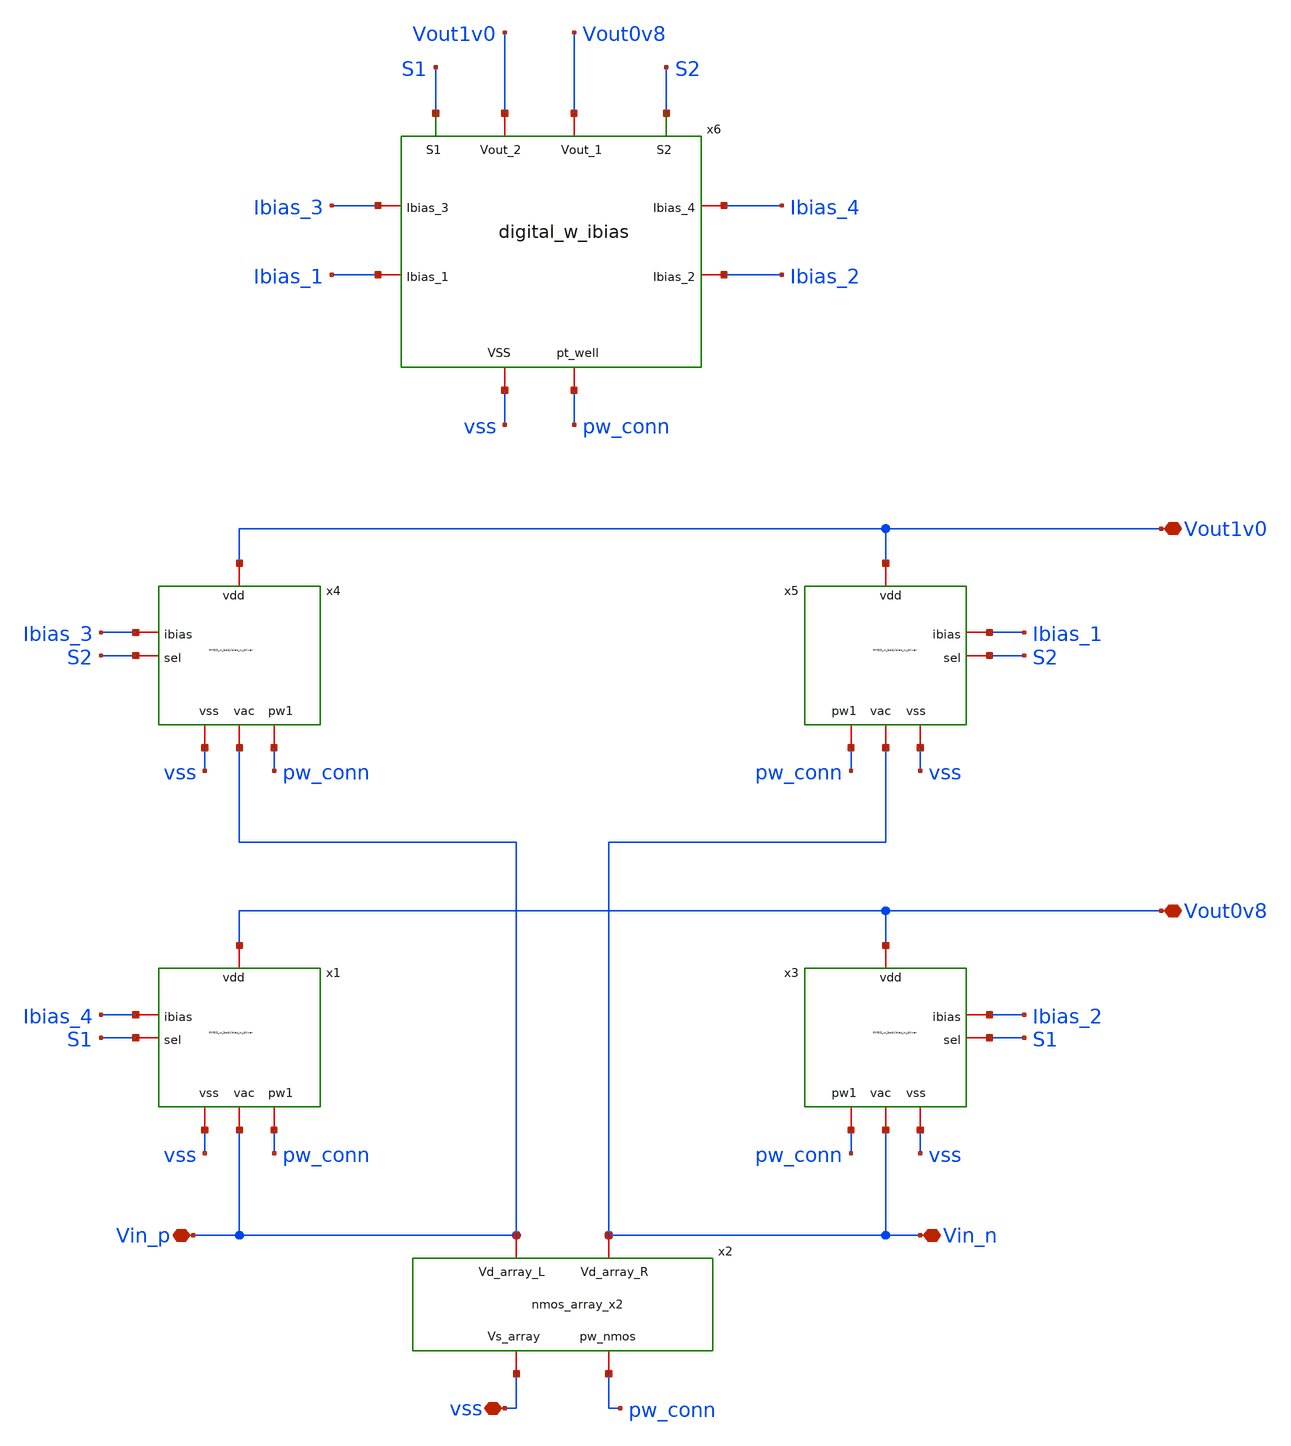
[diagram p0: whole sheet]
** sch_path: Layouts/Top/top_integration_SSDOR.sch
**.subckt top_integration_SSDOR vss Vout0v8 Vout1v0 Vin_n Vin_p
*.iopin vss
*.iopin Vout0v8
*.iopin Vout1v0
*.iopin Vin_n
*.iopin Vin_p
x1 Vout0v8 Vin_p Ibias_4 S1 vss pw_conn PMOS_w_bodybias_w_driver
x2 Vin_p Vin_n pw_conn vss nmos_array_x2
x3 Vout0v8 Vin_n Ibias_2 S1 vss pw_conn PMOS_w_bodybias_w_driver
x4 Vout1v0 Vin_p Ibias_3 S2 vss pw_conn PMOS_w_bodybias_w_driver
x5 Vout1v0 Vin_n Ibias_1 S2 vss pw_conn PMOS_w_bodybias_w_driver
x6 Vout1v0 Vout0v8 S1 vss S2 Ibias_3 Ibias_2 Ibias_4 Ibias_1 pw_conn digital_w_ibias
**.ends

* expanding   symbol:  /shared/designs/Layouts/PMOS/PMOS_w_bodybias_w_driver.sym # of pins=6
** sym_path: Layouts/PMOS/PMOS_w_bodybias_w_driver.sym
** sch_path: Layouts/PMOS/PMOS_w_bodybias_w_driver.sch
.subckt PMOS_w_bodybias_w_driver vdd vac ibias sel vss pw1
*.iopin vdd
*.iopin ibias
*.iopin vac
*.iopin vss
*.iopin sel
*.iopin pw1
XM1 net1 vac vdd net2 sg13_lv_pmos w=9u l=0.13u ng=1 m=1 mm_ok=1
XM2 net1 vdd vac net2 sg13_lv_pmos w=3u l=0.13u ng=1 m=1 mm_ok=1
XR2 net1 net2 ntap1 R=65.77 w=0.7e-6 l=5e-6
XM3 vac net3 vdd net4 sg13_lv_pmos w=86.4u l=0.13u ng=36 m=1 mm_ok=1
XM4 vac net3 vdd net4 sg13_lv_pmos w=86.4u l=0.13u ng=36 m=1 mm_ok=1
XM5 vac net3 vdd net4 sg13_lv_pmos w=86.4u l=0.13u ng=36 m=1 mm_ok=1
XM6 vac net3 vdd net4 sg13_lv_pmos w=86.4u l=0.13u ng=36 m=1 mm_ok=1
XM7 vac net3 vdd net4 sg13_lv_pmos w=86.4u l=0.13u ng=36 m=1 mm_ok=1
XM8 vac net3 vdd net4 sg13_lv_pmos w=86.4u l=0.13u ng=36 m=1 mm_ok=1
XM9 vac net3 vdd net4 sg13_lv_pmos w=86.4u l=0.13u ng=36 m=1 mm_ok=1
XM10 vac net3 vdd net4 sg13_lv_pmos w=86.4u l=0.13u ng=36 m=1 mm_ok=1
XM11 vac net3 vdd net4 sg13_lv_pmos w=86.4u l=0.13u ng=36 m=1 mm_ok=1
XM12 vac net3 vdd net4 sg13_lv_pmos w=86.4u l=0.13u ng=36 m=1 mm_ok=1
XM13 vac net3 vdd net4 sg13_lv_pmos w=86.4u l=0.13u ng=36 m=1 mm_ok=1
XM14 vac net3 vdd net4 sg13_lv_pmos w=86.4u l=0.13u ng=36 m=1 mm_ok=1
XM15 vac net3 vdd net4 sg13_lv_pmos w=86.4u l=0.13u ng=36 m=1 mm_ok=1
XM16 vac net3 vdd net4 sg13_lv_pmos w=86.4u l=0.13u ng=36 m=1 mm_ok=1
XM17 vac net3 vdd net4 sg13_lv_pmos w=86.4u l=0.13u ng=36 m=1 mm_ok=1
XM18 vac net3 vdd net4 sg13_lv_pmos w=86.4u l=0.13u ng=36 m=1 mm_ok=1
XR9 net1 net4 ntap1 R=1.116 w=1e-6 l=292e-6
XR1 net1 net4 ntap1 R=1.116 w=1e-6 l=292e-6
XR3 net1 net4 ntap1 R=1.116 w=1e-6 l=292e-6
XR4 net1 net4 ntap1 R=1.116 w=1e-6 l=292e-6
XR5 net1 net4 ntap1 R=1.116 w=1e-6 l=292e-6
XR6 net1 net4 ntap1 R=1.116 w=1e-6 l=292e-6
XR7 net1 net4 ntap1 R=1.116 w=1e-6 l=292e-6
XR8 net1 net4 ntap1 R=1.116 w=1e-6 l=292e-6
XR10 net1 net4 ntap1 R=1.116 w=1e-6 l=292e-6
XM19 net6 net5 vac nw sg13_lv_pmos w=4u l=0.5u ng=1 m=1 mm_ok=1
XM20 net5 net5 vdd nw sg13_lv_pmos w=4u l=0.5u ng=1 m=1 mm_ok=1
XM21 net7 net8 vdd nw sg13_lv_pmos w=4u l=0.5u ng=1 m=1 mm_ok=1
XM22 net8 net8 vac nw sg13_lv_pmos w=4u l=0.5u ng=1 m=1 mm_ok=1
XM23 net6 net6 vss pw1 sg13_lv_nmos w=1u l=0.5u ng=1 m=1 mm_ok=1
XM24 net7 net6 vss pw1 sg13_lv_nmos w=1u l=0.5u ng=1 m=1 mm_ok=1
XM25 net5 ibias vss pw1 sg13_lv_nmos w=1u l=0.5u ng=1 m=1 mm_ok=1
XM26 ibias ibias vss pw1 sg13_lv_nmos w=1u l=0.5u ng=1 m=1 mm_ok=1
XM27 net8 ibias vss pw1 sg13_lv_nmos w=1u l=0.5u ng=1 m=1 mm_ok=1
XR11 vdd nw ntap1 R=13.24 w=1e-6 l=24e-6
XR12 vdd nw ntap1 R=7.84 w=1.0e-6 l=41e-6
XR13 vdd nw ntap1 R=7.84 w=1.0e-6 l=41e-6
XM28 vdd net10 net9 pw1 sg13_lv_nmos w=1u l=0.13u ng=1 m=1 mm_ok=1
XM29 vdd sel net9 nw sg13_lv_pmos w=2u l=0.13u ng=1 m=1 mm_ok=1
XM30 net7 sel net9 pw1 sg13_lv_nmos w=1u l=0.13u ng=1 m=1 mm_ok=1
XM31 net7 net10 net9 nw sg13_lv_pmos w=2u l=0.13u ng=1 m=1 mm_ok=1
XM32 net11 net9 vss pw1 sg13_lv_nmos w=1u l=0.13u ng=1 m=1 mm_ok=1
XM33 net11 net9 vdd nw sg13_lv_pmos w=1u l=0.13u ng=1 m=2 mm_ok=1
XM34 net12 net11 vss pw1 sg13_lv_nmos w=1u l=0.13u ng=1 m=2 mm_ok=1
XM35 net12 net11 vdd nw sg13_lv_pmos w=1u l=0.13u ng=1 m=4 mm_ok=1
XM36 net13 net12 vss pw1 sg13_lv_nmos w=1u l=0.13u ng=1 m=8 mm_ok=1
XM37 net13 net12 vdd nw sg13_lv_pmos w=1u l=0.13u ng=1 m=16 mm_ok=1
XM38 net3 net13 vdd nw sg13_lv_pmos w=1u l=0.13u ng=1 m=54 mm_ok=1
XM39 net3 net13 vss pw1 sg13_lv_nmos w=1u l=0.13u ng=1 m=27 mm_ok=1
XR14 vdd nw ntap1 R=89.09 w=3e-6 l=1e-6
XR15 vdd nw ntap1 R=196 w=1e-6 l=1e-6
XR16 vdd nw ntap1 R=122.5 w=2e-6 l=1e-6
XR17 vdd nw ntap1 R=122.5 w=2e-6 l=1e-6
XR18 vss pw1 ptap1 R=13.8 w=23.0e-6 l=1.0e-6
XR19 vss pw1 ptap1 R=20.85 w=1.0e-6 l=15.0e-6
XR20 vss pw1 ptap1 R=14.41 w=1.0e-6 l=22.0e-6
XR21 vss pw1 ptap1 R=14.41 w=1.0e-6 l=22.0e-6
XM40 net10 sel vss pw1 sg13_lv_nmos w=0.5u l=0.13u ng=1 m=1 mm_ok=1
XM41 net10 sel vdd nw sg13_lv_pmos w=1u l=0.13u ng=1 m=1 mm_ok=1
.ends


* expanding   symbol:  /shared/designs/Layouts/PMOS/nmos_array_x2.sym # of pins=4
** sym_path: Layouts/PMOS/nmos_array_x2.sym
** sch_path: Layouts/PMOS/nmos_array_x2.sch
.subckt nmos_array_x2 Vd_array_L Vd_array_R pw_nmos Vs_array
*.iopin Vd_array_L
*.iopin Vd_array_R
*.iopin pw_nmos
*.iopin Vs_array
XM2 Vd_array_L Vd_array_R Vs_array pw_nmos sg13_lv_nmos w=86.4u l=0.13u ng=36 m=1 mm_ok=1
XR2 Vs_array pw_nmos ptap1 R=1.529 w=1e-6 l=213e-6
XM1 Vd_array_L Vd_array_R Vs_array pw_nmos sg13_lv_nmos w=86.4u l=0.13u ng=36 m=1 mm_ok=1
XM3 Vd_array_L Vd_array_R Vs_array pw_nmos sg13_lv_nmos w=86.4u l=0.13u ng=36 m=1 mm_ok=1
XM4 Vd_array_L Vd_array_R Vs_array pw_nmos sg13_lv_nmos w=86.4u l=0.13u ng=36 m=1 mm_ok=1
XM5 Vd_array_L Vd_array_R Vs_array pw_nmos sg13_lv_nmos w=86.4u l=0.13u ng=36 m=1 mm_ok=1
XM6 Vd_array_L Vd_array_R Vs_array pw_nmos sg13_lv_nmos w=86.4u l=0.13u ng=36 m=1 mm_ok=1
XM7 Vd_array_L Vd_array_R Vs_array pw_nmos sg13_lv_nmos w=86.4u l=0.13u ng=36 m=1 mm_ok=1
XM8 Vd_array_L Vd_array_R Vs_array pw_nmos sg13_lv_nmos w=86.4u l=0.13u ng=36 m=1 mm_ok=1
XM9 Vd_array_L Vd_array_R Vs_array pw_nmos sg13_lv_nmos w=86.4u l=0.13u ng=36 m=1 mm_ok=1
XR1 Vs_array pw_nmos ptap1 R=1.529 w=1e-6 l=213e-6
XR3 Vs_array pw_nmos ptap1 R=1.529 w=1e-6 l=213e-6
XR4 Vs_array pw_nmos ptap1 R=1.529 w=1e-6 l=213e-6
XR5 Vs_array pw_nmos ptap1 R=1.529 w=1e-6 l=213e-6
XR6 Vs_array pw_nmos ptap1 R=1.529 w=1e-6 l=213e-6
XR7 Vs_array pw_nmos ptap1 R=1.529 w=1e-6 l=213e-6
XM10 Vd_array_R Vd_array_L Vs_array pw_nmos sg13_lv_nmos w=86.4u l=0.13u ng=36 m=1 mm_ok=1
XR8 Vs_array pw_nmos ptap1 R=1.529 w=1e-6 l=213e-6
XM11 Vd_array_R Vd_array_L Vs_array pw_nmos sg13_lv_nmos w=86.4u l=0.13u ng=36 m=1 mm_ok=1
XM12 Vd_array_R Vd_array_L Vs_array pw_nmos sg13_lv_nmos w=86.4u l=0.13u ng=36 m=1 mm_ok=1
XM13 Vd_array_R Vd_array_L Vs_array pw_nmos sg13_lv_nmos w=86.4u l=0.13u ng=36 m=1 mm_ok=1
XM14 Vd_array_R Vd_array_L Vs_array pw_nmos sg13_lv_nmos w=86.4u l=0.13u ng=36 m=1 mm_ok=1
XM15 Vd_array_R Vd_array_L Vs_array pw_nmos sg13_lv_nmos w=86.4u l=0.13u ng=36 m=1 mm_ok=1
XM16 Vd_array_R Vd_array_L Vs_array pw_nmos sg13_lv_nmos w=86.4u l=0.13u ng=36 m=1 mm_ok=1
XM17 Vd_array_R Vd_array_L Vs_array pw_nmos sg13_lv_nmos w=86.4u l=0.13u ng=36 m=1 mm_ok=1
XM18 Vd_array_R Vd_array_L Vs_array pw_nmos sg13_lv_nmos w=86.4u l=0.13u ng=36 m=1 mm_ok=1
XR9 Vs_array pw_nmos ptap1 R=1.529 w=1e-6 l=213e-6
XR10 Vs_array pw_nmos ptap1 R=1.529 w=1e-6 l=213e-6
XR11 Vs_array pw_nmos ptap1 R=1.529 w=1e-6 l=213e-6
XR12 Vs_array pw_nmos ptap1 R=1.529 w=1e-6 l=213e-6
XR13 Vs_array pw_nmos ptap1 R=1.529 w=1e-6 l=213e-6
XR14 Vs_array pw_nmos ptap1 R=1.529 w=1e-6 l=213e-6
.ends


* expanding   symbol:  /shared/designs/Layouts/digital_w_ibias/digital_w_ibias.sym # of pins=10
** sym_path: Layouts/digital_w_ibias/digital_w_ibias.sym
** sch_path: Layouts/digital_w_ibias/digital_w_ibias.sch
.subckt digital_w_ibias Vout_2 Vout_1 S1 VSS S2 Ibias_3 Ibias_2 Ibias_4 Ibias_1 pt_well
*.iopin Ibias_1
*.iopin Ibias_2
*.iopin Ibias_3
*.iopin Ibias_4
*.iopin VSS
*.iopin Vout_2
*.opin S2
*.opin S1
*.iopin Vout_1
*.iopin pt_well
XM1 net8 net3 Vout_2 net14 sg13_lv_pmos w=1u l=2u ng=1 m=1 mm_ok=1
XM2 net11 net3 Vout_2 net14 sg13_lv_pmos w=1u l=2u ng=1 m=6 mm_ok=1
XM3 net11 net1 Vout_2 net14 sg13_lv_pmos w=1u l=2u ng=1 m=6 mm_ok=1
XM4 net10 net1 Vout_2 net14 sg13_lv_pmos w=1u l=2u ng=1 m=1 mm_ok=1
XM12 net7 net3 Vout_2 net14 sg13_lv_pmos w=1u l=2u ng=1 m=1 mm_ok=1
XM13 net5 net3 Vout_2 net14 sg13_lv_pmos w=1u l=2u ng=1 m=1 mm_ok=1
XM5 net9 net1 Vout_2 net14 sg13_lv_pmos w=1u l=2u ng=1 m=1 mm_ok=1
XM7 net4 net5 net6 pt_well sg13_lv_nmos w=0.5u l=1.2u ng=1 m=1 mm_ok=1
XM10 net6 net7 VSS pt_well sg13_lv_nmos w=0.5u l=1.2u ng=1 m=1 mm_ok=1
XM11 net7 net7 net6 pt_well sg13_lv_nmos w=10u l=0.26u ng=1 m=30 mm_ok=1
XM16 net5 net5 net4 pt_well sg13_lv_nmos w=10u l=0.26u ng=1 m=30 mm_ok=1
XM24 VSS VSS net2 net12 sg13_lv_pmos w=10u l=0.36u ng=1 m=20 mm_ok=1
XM25 net2 VSS net10 net12 sg13_lv_pmos w=10u l=0.36u ng=1 m=1 mm_ok=1
XR1 net9 net13 VSS rppd w=0.5e-6 l=1170e-6 m=1 b=0 mm_ok=1
XR3 net13 VSS VSS rhigh w=0.5e-6 l=27e-6 m=1 b=0 mm_ok=1
XR10 net8 VSS VSS rppd w=0.5e-6 l=2110e-6 m=1 b=0 mm_ok=1
XM6 Vout_2 Vout_2 Vout_2 net14 sg13_lv_pmos w=1u l=2u ng=1 m=1 mm_ok=1
XM8 net15 net8 VSS pt_well sg13_lv_nmos w=10u l=8u ng=1 m=6 mm_ok=1
XM9 net15 net15 Vout_2 net16 sg13_lv_pmos w=10u l=0.5u ng=1 m=4 mm_ok=1
XM14 net3 net15 Vout_2 net16 sg13_lv_pmos w=10u l=0.5u ng=1 m=4 mm_ok=1
XM15 net3 net4 VSS pt_well sg13_lv_nmos w=10u l=8u ng=1 m=6 mm_ok=1
XR2 Vout_2 net16 ntap1 R=15.81 w=1e-6 l=20e-6
XR4_opamp VSS pt_well ptap1 R=5.765 w=56e-6 l=1e-6
XM17 net17 net9 VSS pt_well sg13_lv_nmos w=10u l=8u ng=1 m=6 mm_ok=1
XM18 net17 net17 Vout_2 net18 sg13_lv_pmos w=10u l=0.5u ng=1 m=4 mm_ok=1
XM19 net1 net17 Vout_2 net18 sg13_lv_pmos w=10u l=0.5u ng=1 m=4 mm_ok=1
XM20 net1 net2 VSS pt_well sg13_lv_nmos w=10u l=8u ng=1 m=6 mm_ok=1
XR5 Vout_2 net18 ntap1 R=15.81 w=1e-6 l=20e-6
XR6_opamp VSS pt_well ptap1 R=5.765 w=56e-6 l=1e-6
XR7 Vout_2 net14 ntap1 R=57.65 w=5e-6 l=1e-6
XR8 Vout_2 net14 ntap1 R=57.65 w=5e-6 l=1e-6
XR9 Vout_2 net12 ntap1 R=37.69 w=1e-6 l=8e-6
XR11_PTAT VSS pt_well ptap1 R=16.61 w=1e-6 l=19e-6
XM30 net11 net11 VSS pt_well sg13_lv_nmos w=1.1u l=2u ng=1 m=3 mm_ok=1
XR4 net20 Vb0v5 VSS rppd w=0.5e-6 l=972.9e-6 m=1 b=0 mm_ok=1
XR6 net21 Vb0v4 VSS rppd w=0.5e-6 l=1167.4e-6 m=1 b=0 mm_ok=1
XM21 net19 net11 VSS pt_well sg13_lv_nmos w=1.1u l=2u ng=1 m=3 mm_ok=1
XM23 net19 net19 Vout_2 net22 sg13_lv_pmos w=1.1u l=2u ng=1 m=6 mm_ok=1
XM22 Ibias_1 net19 Vout_2 net22 sg13_lv_pmos w=1.1u l=2u ng=1 m=6 mm_ok=1
XM26 Ibias_2 net19 Vout_2 net22 sg13_lv_pmos w=1.1u l=2u ng=1 m=6 mm_ok=1
XM27 Ibias_3 net19 Vout_2 net22 sg13_lv_pmos w=1.1u l=2u ng=1 m=6 mm_ok=1
XM28 Ibias_4 net19 Vout_2 net22 sg13_lv_pmos w=1.1u l=2u ng=1 m=6 mm_ok=1
XM29 Ibias_5 net19 Vout_2 net22 sg13_lv_pmos w=1.1u l=2u ng=1 m=6 mm_ok=1
XM31 Ibias_6 net19 Vout_2 net22 sg13_lv_pmos w=1.1u l=2u ng=1 m=6 mm_ok=1
XC5 net11 VSS cap_cmim w=18e-6 l=18e-6 m=9 mm_ok=1
XC2 net19 Vout_2 cap_cmim w=2.6e-6 l=2.6e-6 m=1 mm_ok=1
XR11 Vout_2 net22 ntap1 R=55.68 w=6e-6 l=0.7e-6
XR12 Vout_2 net22 ntap1 R=55.68 w=6e-6 l=0.7e-6
XR13 Vout_2 net22 ntap1 R=55.68 w=6e-6 l=0.7e-6
XR14 Vout_2 net22 ntap1 R=55.68 w=6e-6 l=0.7e-6
XR15 Vout_2 net22 ntap1 R=55.68 w=6e-6 l=0.7e-6
XR16 Vout_2 net22 ntap1 R=55.68 w=6e-6 l=0.7e-6
XR17 Vout_2 net22 ntap1 R=55.68 w=6e-6 l=0.7e-6
XR18 Vout_2 net22 ntap1 R=55.68 w=6e-6 l=0.7e-6
XR19 Vout_2 net22 ntap1 R=55.68 w=6e-6 l=0.7e-6
XR20 VSS pt_well ptap1 R=57.65 w=1e-6 l=5e-6
XM32 net20 net19 Vout_2 net22 sg13_lv_pmos w=1.1u l=2u ng=1 m=6 mm_ok=1
XM33 net21 net19 Vout_2 net22 sg13_lv_pmos w=1.1u l=2u ng=1 m=6 mm_ok=1
XR21 Vb0v5 VSS VSS rppd w=0.5e-6 l=994e-6 m=1 b=0 mm_ok=1
XR22 Vb0v4 VSS VSS rppd w=0.5e-6 l=792e-6 m=1 b=0 mm_ok=1
XM34 net23 net23 Vout_2 wellb1 sg13_lv_pmos w=0.5u l=0.13u ng=1 m=1 mm_ok=1
XM35 net24 net23 Vout_2 wellb1 sg13_lv_pmos w=0.5u l=0.13u ng=1 m=1 mm_ok=1
XM36 net23 net24 Vout_2 wellb1 sg13_lv_pmos w=0.5u l=0.13u ng=1 m=1 mm_ok=1
XM37 net24 net24 Vout_2 wellb1 sg13_lv_pmos w=0.5u l=0.13u ng=1 m=1 mm_ok=1
XM38 net23 Vb0v4 net27 pt_well sg13_lv_nmos w=5u l=0.5u ng=1 m=1 mm_ok=1
XM39 net24 Vx1 net27 pt_well sg13_lv_nmos w=5u l=0.5u ng=1 m=1 mm_ok=1
XM40 net27 Ibias_5 VSS pt_well sg13_lv_nmos w=1u l=0.5u ng=1 m=1 mm_ok=1
XM41 net26 net23 Vout_2 wellb1 sg13_lv_pmos w=2u l=0.5u ng=1 m=1 mm_ok=1
XM42 net25 net24 Vout_2 wellb1 sg13_lv_pmos w=2u l=0.5u ng=1 m=1 mm_ok=1
XM43 net25 net26 VSS pt_well sg13_lv_nmos w=1u l=0.5u ng=1 m=1 mm_ok=1
XM44 net26 net26 VSS pt_well sg13_lv_nmos w=1u l=0.5u ng=1 m=1 mm_ok=1
XM45 Ibias_5 Ibias_5 VSS pt_well sg13_lv_nmos w=1u l=0.5u ng=1 m=1 mm_ok=1
XM46 net28 net25 VSS pt_well sg13_lv_nmos w=1u l=0.13u ng=1 m=1 mm_ok=1
XM47 net28 net25 Vout_2 wellb1 sg13_lv_pmos w=1u l=0.13u ng=1 m=2 mm_ok=1
XM48 net29 net28 VSS pt_well sg13_lv_nmos w=2u l=0.13u ng=1 m=1 mm_ok=1
XM49 net29 net28 Vout_2 wellb1 sg13_lv_pmos w=2u l=0.13u ng=1 m=2 mm_ok=1
XM50 X net29 VSS pt_well sg13_lv_nmos w=3u l=0.13u ng=1 m=1 mm_ok=1
XM51 X net29 Vout_2 wellb1 sg13_lv_pmos w=3u l=0.13u ng=1 m=2 mm_ok=1
XM52 net30 net30 Vout_2 wellb1 sg13_lv_pmos w=0.5u l=0.13u ng=1 m=1 mm_ok=1
XM53 net31 net30 Vout_2 wellb1 sg13_lv_pmos w=0.5u l=0.13u ng=1 m=1 mm_ok=1
XM54 net30 net31 Vout_2 wellb1 sg13_lv_pmos w=0.5u l=0.13u ng=1 m=1 mm_ok=1
XM55 net31 net31 Vout_2 wellb1 sg13_lv_pmos w=0.5u l=0.13u ng=1 m=1 mm_ok=1
XM56 net30 Vb0v5 net34 pt_well sg13_lv_nmos w=5u l=0.5u ng=1 m=1 mm_ok=1
XM57 net31 Vx2 net34 pt_well sg13_lv_nmos w=5u l=0.5u ng=1 m=1 mm_ok=1
XM58 net34 Ibias_6 VSS pt_well sg13_lv_nmos w=1u l=0.5u ng=1 m=1 mm_ok=1
XM59 net33 net30 Vout_2 wellb1 sg13_lv_pmos w=2u l=0.5u ng=1 m=1 mm_ok=1
XM60 net32 net31 Vout_2 wellb1 sg13_lv_pmos w=2u l=0.5u ng=1 m=1 mm_ok=1
XM61 net32 net33 VSS pt_well sg13_lv_nmos w=1u l=0.5u ng=1 m=1 mm_ok=1
XM62 net33 net33 VSS pt_well sg13_lv_nmos w=1u l=0.5u ng=1 m=1 mm_ok=1
XM63 Ibias_6 Ibias_6 VSS pt_well sg13_lv_nmos w=1u l=0.5u ng=1 m=1 mm_ok=1
XM64 net35 net32 VSS pt_well sg13_lv_nmos w=1u l=0.13u ng=1 m=1 mm_ok=1
XM65 net35 net32 Vout_2 wellb1 sg13_lv_pmos w=1u l=0.13u ng=1 m=2 mm_ok=1
XM66 net36 net35 VSS pt_well sg13_lv_nmos w=2u l=0.13u ng=1 m=1 mm_ok=1
XM67 net36 net35 Vout_2 wellb1 sg13_lv_pmos w=2u l=0.13u ng=1 m=2 mm_ok=1
XM68 Y net36 VSS pt_well sg13_lv_nmos w=3u l=0.13u ng=1 m=1 mm_ok=1
XM69 Y net36 Vout_2 wellb1 sg13_lv_pmos w=3u l=0.13u ng=1 m=2 mm_ok=1
XM70 Vx1 Vx1 Vout_1 wellu sg13_lv_pmos w=0.5u l=10u ng=1 m=19 mm_ok=1
XM71 Vx1 Vx1 VSS pt_well sg13_lv_nmos w=0.5u l=10u ng=1 m=1 mm_ok=1
XM72 Vx2 Vx2 Vout_2 welld sg13_lv_pmos w=0.5u l=10u ng=1 m=10 mm_ok=1
XM73 Vx2 Vx2 VSS pt_well sg13_lv_nmos w=0.5u l=10u ng=1 m=1 mm_ok=1
XR23 Vout_2 wellb1 ntap1 R=25.79 w=12.0e-6 l=1.0e-6
XR24 Vout_2 wellb1 ntap1 R=25.79 w=12.0e-6 l=1.0e-6
XR25 Vout_1 wellu ntap1 R=30.62 w=10.0e-6 l=1.0e-6
XR26 Vout_2 welld ntap1 R=30.62 w=10.0e-6 l=1.0e-6
XM74 net37 net38 VSS pt_well sg13_lv_nmos w=2u l=1u ng=1 m=1 mm_ok=1
XM75 net37 net38 Vout_2 well sg13_lv_pmos w=4u l=1u ng=1 m=1 mm_ok=1
XM76 net39 net37 VSS pt_well sg13_lv_nmos w=2u l=1u ng=1 m=1 mm_ok=1
XM77 net39 net37 Vout_2 well sg13_lv_pmos w=4u l=1u ng=1 m=1 mm_ok=1
XM78 net40 net39 VSS pt_well sg13_lv_nmos w=2u l=1u ng=1 m=1 mm_ok=1
XM79 net40 net39 Vout_2 well sg13_lv_pmos w=4u l=1u ng=1 m=1 mm_ok=1
XM80 net41 net40 VSS pt_well sg13_lv_nmos w=2u l=1u ng=1 m=1 mm_ok=1
XM81 net41 net40 Vout_2 well sg13_lv_pmos w=4u l=1u ng=1 m=1 mm_ok=1
XM82 net42 net41 VSS pt_well sg13_lv_nmos w=2u l=1u ng=1 m=1 mm_ok=1
XM83 net42 net41 Vout_2 well sg13_lv_pmos w=4u l=1u ng=1 m=1 mm_ok=1
XM84 net43 net42 VSS pt_well sg13_lv_nmos w=2u l=1u ng=1 m=1 mm_ok=1
XM85 net43 net42 Vout_2 well sg13_lv_pmos w=4u l=1u ng=1 m=1 mm_ok=1
XM86 net44 net43 VSS pt_well sg13_lv_nmos w=2u l=1u ng=1 m=1 mm_ok=1
XM87 net44 net43 Vout_2 well sg13_lv_pmos w=4u l=1u ng=1 m=1 mm_ok=1
XM88 net45 net44 VSS pt_well sg13_lv_nmos w=2u l=1u ng=1 m=1 mm_ok=1
XM89 net45 net44 Vout_2 well sg13_lv_pmos w=4u l=1u ng=1 m=1 mm_ok=1
XM90 net46 net45 VSS pt_well sg13_lv_nmos w=2u l=1u ng=1 m=1 mm_ok=1
XM91 net46 net45 Vout_2 well sg13_lv_pmos w=4u l=1u ng=1 m=1 mm_ok=1
XM92 net47 net46 VSS pt_well sg13_lv_nmos w=2u l=1u ng=1 m=1 mm_ok=1
XM93 net47 net46 Vout_2 well sg13_lv_pmos w=4u l=1u ng=1 m=1 mm_ok=1
XM94 net38 net47 VSS pt_well sg13_lv_nmos w=2u l=1u ng=1 m=1 mm_ok=1
XM95 net38 net47 Vout_2 well sg13_lv_pmos w=4u l=1u ng=1 m=1 mm_ok=1
XM96 net48 net38 VSS pt_well sg13_lv_nmos w=2u l=0.13u ng=1 m=1 mm_ok=1
XM97 net48 net38 Vout_2 well sg13_lv_pmos w=4u l=0.13u ng=1 m=1 mm_ok=1
XM98 net49 net48 Vout_2 well sg13_lv_pmos w=8u l=0.13u ng=2 m=1 mm_ok=1
XM99 net49 net48 VSS pt_well sg13_lv_nmos w=4u l=0.13u ng=2 m=1 mm_ok=1
XR27 Vout_2 well ntap1 R=11.01 w=29.0e-6 l=1.0e-6
XM100 net51 X Vout_2 well sg13_lv_pmos w=2u l=0.13u ng=1 m=1 mm_ok=1
XM101 net51 net49 Vout_2 well sg13_lv_pmos w=2u l=0.13u ng=1 m=1 mm_ok=1
XM102 net51 X net53 pt_well sg13_lv_nmos w=1u l=0.13u ng=1 m=1 mm_ok=1
XM103 net53 net49 VSS pt_well sg13_lv_nmos w=1u l=0.13u ng=1 m=1 mm_ok=1
XM104 net50 net51 Vout_2 well sg13_lv_pmos w=2u l=0.13u ng=1 m=1 mm_ok=1
XM105 net50 net51 VSS pt_well sg13_lv_nmos w=1u l=0.13u ng=1 m=1 mm_ok=1
XM106 net52 Y Vout_2 well sg13_lv_pmos w=2u l=0.13u ng=1 m=1 mm_ok=1
XM107 net52 Y VSS pt_well sg13_lv_nmos w=1u l=0.13u ng=1 m=1 mm_ok=1
XM108 net54 net52 Vout_2 well sg13_lv_pmos w=2u l=0.13u ng=1 m=1 mm_ok=1
XM109 S2 net49 net54 well sg13_lv_pmos w=2u l=0.13u ng=1 m=1 mm_ok=1
XM110 S2 net52 VSS pt_well sg13_lv_nmos w=1u l=0.13u ng=1 m=1 mm_ok=1
XM111 S2 net49 VSS pt_well sg13_lv_nmos w=1u l=0.13u ng=1 m=1 mm_ok=1
XR28 Vout_2 well ntap1 R=42.61 w=7.0e-6 l=1.0e-6
XM112 net55 net50 Vout_1 well_1 sg13_lv_pmos w=2u l=0.13u ng=1 m=1 mm_ok=1
XM113 net55 net50 VSS pt_well sg13_lv_nmos w=1u l=0.13u ng=1 m=1 mm_ok=1
XM114 S1 net55 Vout_1 well_1 sg13_lv_pmos w=2u l=0.13u ng=1 m=1 mm_ok=1
XM115 S1 net55 VSS pt_well sg13_lv_nmos w=1u l=0.13u ng=1 m=1 mm_ok=1
XR29 Vout_1 well_1 ntap1 R=122.5 w=2.0e-6 l=1.0e-6
XR30 VSS pt_well ptap1 R=23.9 w=13e-6 l=1e-6
XR32 VSS pt_well ptap1 R=30.62 w=10e-6 l=1e-6
XR34 VSS pt_well ptap1 R=11.01 w=29e-6 l=1e-6
XR35 VSS pt_well ptap1 R=89.09 w=3e-6 l=1e-6
XR36 VSS pt_well ptap1 R=42.61 w=7e-6 l=1e-6
XR31 VSS pt_well ptap1 R=23.9 w=13e-6 l=1e-6
XR33 VSS pt_well ptap1 R=30.62 w=10e-6 l=1e-6
.ends

.end
